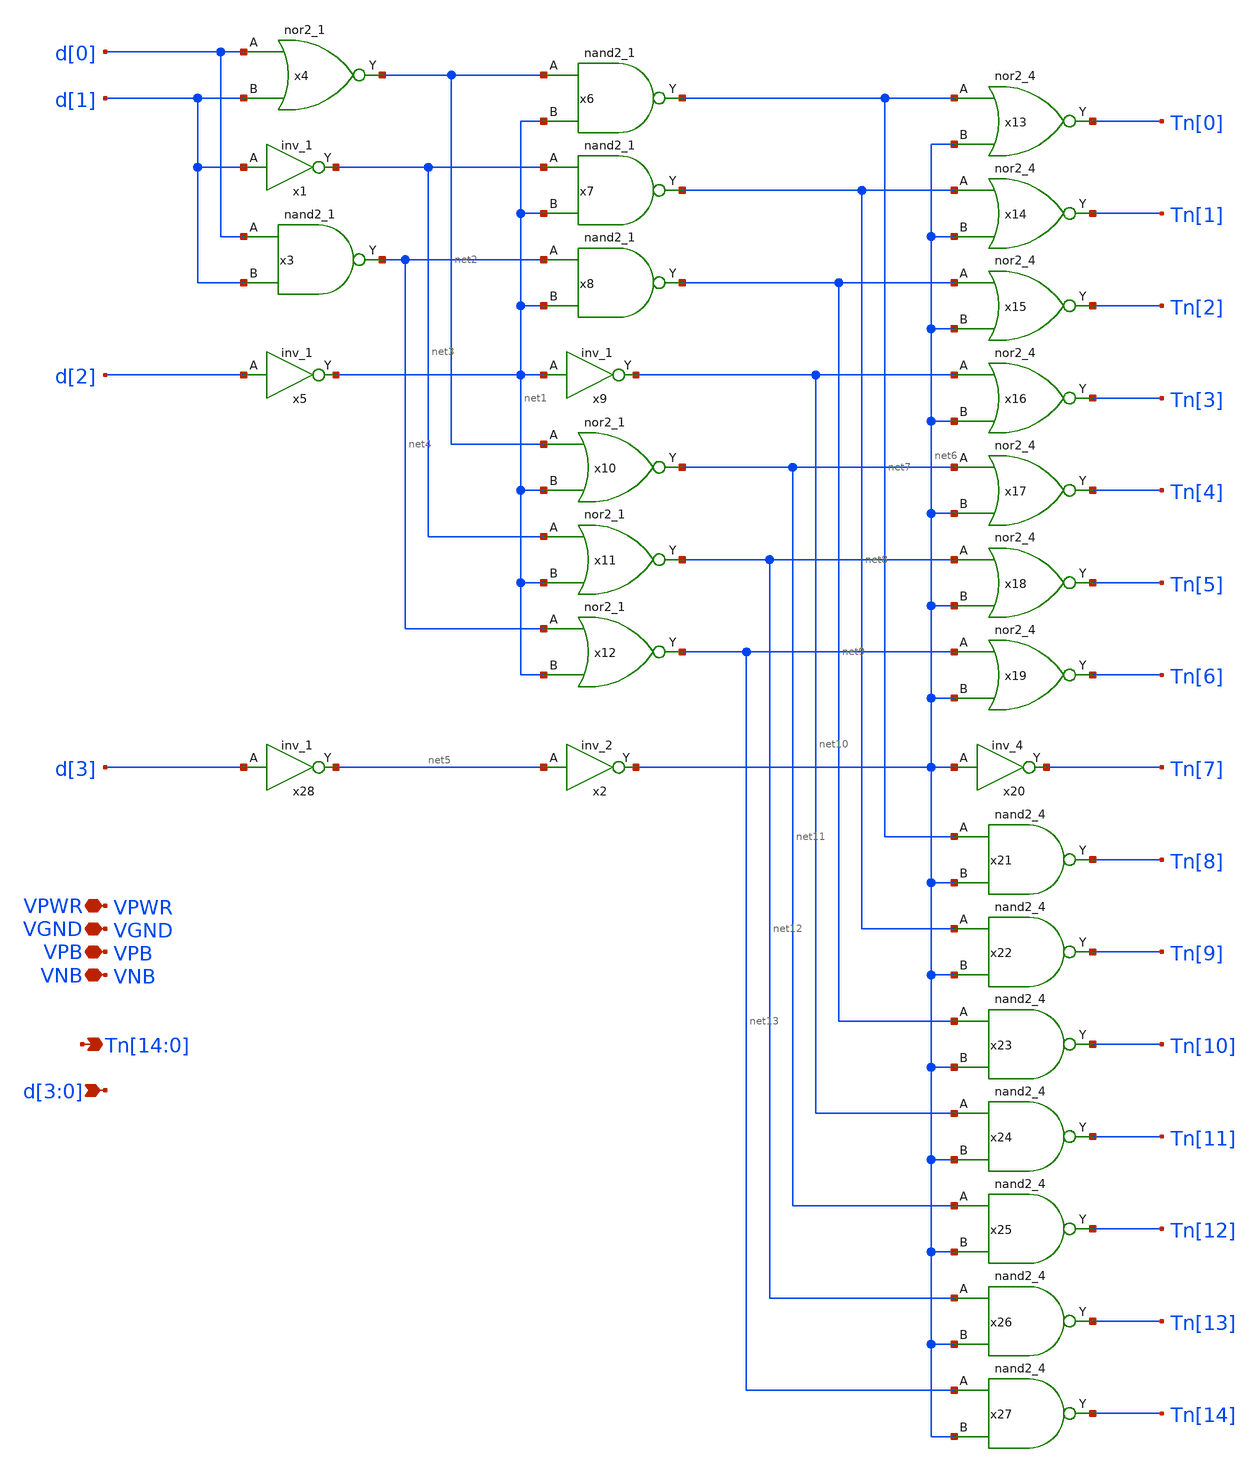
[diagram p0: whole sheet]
** sch_path: xschem/thermo15.sch
**.subckt thermo15 VPWR d[3],d[2],d[1],d[0] VGND VPB VNB
*+ Tn[14],Tn[13],Tn[12],Tn[11],Tn[10],Tn[9],Tn[8],Tn[7],Tn[6],Tn[5],Tn[4],Tn[3],Tn[2],Tn[1],Tn[0]
*.iopin VPWR
*.ipin d[3],d[2],d[1],d[0]
*.iopin VGND
*.iopin VPB
*.iopin VNB
*.opin
*+ Tn[14],Tn[13],Tn[12],Tn[11],Tn[10],Tn[9],Tn[8],Tn[7],Tn[6],Tn[5],Tn[4],Tn[3],Tn[2],Tn[1],Tn[0]
x1 d[1] VGND VNB VPB VPWR net3 sky130_fd_sc_hd__inv_1
x2 net5 VGND VNB VPB VPWR net6 sky130_fd_sc_hd__inv_2
x3 d[0] d[1] VGND VNB VPB VPWR net4 sky130_fd_sc_hd__nand2_1
x4 d[0] d[1] VGND VNB VPB VPWR net2 sky130_fd_sc_hd__nor2_1
x5 d[2] VGND VNB VPB VPWR net1 sky130_fd_sc_hd__inv_1
x6 net2 net1 VGND VNB VPB VPWR net7 sky130_fd_sc_hd__nand2_1
x7 net3 net1 VGND VNB VPB VPWR net8 sky130_fd_sc_hd__nand2_1
x8 net4 net1 VGND VNB VPB VPWR net9 sky130_fd_sc_hd__nand2_1
x9 net1 VGND VNB VPB VPWR net10 sky130_fd_sc_hd__inv_1
x10 net2 net1 VGND VNB VPB VPWR net11 sky130_fd_sc_hd__nor2_1
x11 net3 net1 VGND VNB VPB VPWR net12 sky130_fd_sc_hd__nor2_1
x12 net4 net1 VGND VNB VPB VPWR net13 sky130_fd_sc_hd__nor2_1
x13 net7 net6 VGND VNB VPB VPWR Tn[0] sky130_fd_sc_hd__nor2_4
x14 net8 net6 VGND VNB VPB VPWR Tn[1] sky130_fd_sc_hd__nor2_4
x15 net9 net6 VGND VNB VPB VPWR Tn[2] sky130_fd_sc_hd__nor2_4
x16 net10 net6 VGND VNB VPB VPWR Tn[3] sky130_fd_sc_hd__nor2_4
x17 net11 net6 VGND VNB VPB VPWR Tn[4] sky130_fd_sc_hd__nor2_4
x18 net12 net6 VGND VNB VPB VPWR Tn[5] sky130_fd_sc_hd__nor2_4
x19 net13 net6 VGND VNB VPB VPWR Tn[6] sky130_fd_sc_hd__nor2_4
x20 net6 VGND VNB VPB VPWR Tn[7] sky130_fd_sc_hd__inv_4
x21 net7 net6 VGND VNB VPB VPWR Tn[8] sky130_fd_sc_hd__nand2_4
x22 net8 net6 VGND VNB VPB VPWR Tn[9] sky130_fd_sc_hd__nand2_4
x23 net9 net6 VGND VNB VPB VPWR Tn[10] sky130_fd_sc_hd__nand2_4
x24 net10 net6 VGND VNB VPB VPWR Tn[11] sky130_fd_sc_hd__nand2_4
x25 net11 net6 VGND VNB VPB VPWR Tn[12] sky130_fd_sc_hd__nand2_4
x26 net12 net6 VGND VNB VPB VPWR Tn[13] sky130_fd_sc_hd__nand2_4
x27 net13 net6 VGND VNB VPB VPWR Tn[14] sky130_fd_sc_hd__nand2_4
x28 d[3] VGND VNB VPB VPWR net5 sky130_fd_sc_hd__inv_1
**.ends
.end
